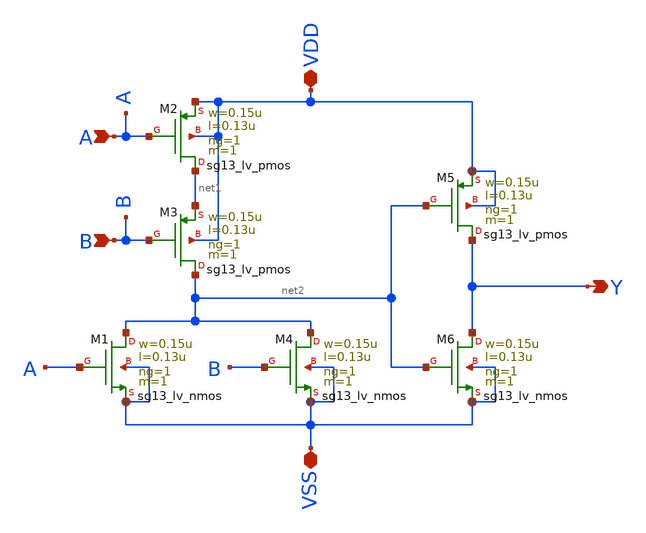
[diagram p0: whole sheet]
** sch_path: logic_gate/OR2/LAYOUT_POST-SIMULATION/OR2.sch
**.subckt OR2 A B Y VDD VSS
*.ipin A
*.ipin B
*.opin Y
*.iopin VDD
*.iopin VSS
XM1 net2 A VSS VSS sg13_lv_nmos w=0.15u l=0.13u ng=1 m=1 mm_ok=1
XM2 net1 A VDD VDD sg13_lv_pmos w=0.15u l=0.13u ng=1 m=1 mm_ok=1
XM3 net2 B net1 VDD sg13_lv_pmos w=0.15u l=0.13u ng=1 m=1 mm_ok=1
XM4 net2 B VSS VSS sg13_lv_nmos w=0.15u l=0.13u ng=1 m=1 mm_ok=1
XM5 Y net2 VDD VDD sg13_lv_pmos w=0.15u l=0.13u ng=1 m=1 mm_ok=1
XM6 Y net2 VSS VSS sg13_lv_nmos w=0.15u l=0.13u ng=1 m=1 mm_ok=1
**.ends
.end
